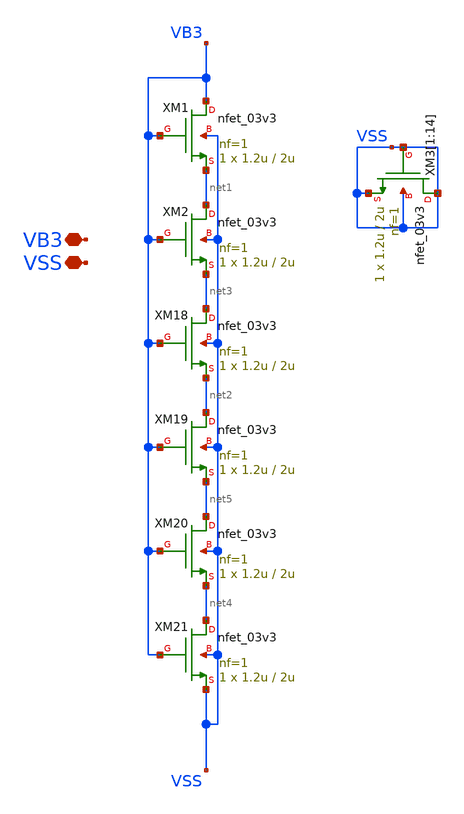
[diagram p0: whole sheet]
** sch_path: TIA_Filter/Folded/FC_bias_vb3.sch
**.subckt FC_bias_vb3 VSS VB3
*.iopin VSS
*.iopin VB3
XM1 VB3 VB3 net1 VSS nfet_03v3 L=2u W=1.2u nf=1 ad='int((nf+1)/2) * W/nf * 0.18u' as='int((nf+2)/2) * W/nf * 0.18u'
+ pd='2*int((nf+1)/2) * (W/nf + 0.18u)' ps='2*int((nf+2)/2) * (W/nf + 0.18u)' nrd='0.18u / W' nrs='0.18u / W'
+ sa=0 sb=0 sd=0 m=1
XM2 net1 VB3 net3 VSS nfet_03v3 L=2u W=1.2u nf=1 ad='int((nf+1)/2) * W/nf * 0.18u' as='int((nf+2)/2) * W/nf * 0.18u'
+ pd='2*int((nf+1)/2) * (W/nf + 0.18u)' ps='2*int((nf+2)/2) * (W/nf + 0.18u)' nrd='0.18u / W' nrs='0.18u / W'
+ sa=0 sb=0 sd=0 m=1
XM18 net3 VB3 net2 VSS nfet_03v3 L=2u W=1.2u nf=1 ad='int((nf+1)/2) * W/nf * 0.18u' as='int((nf+2)/2) * W/nf * 0.18u'
+ pd='2*int((nf+1)/2) * (W/nf + 0.18u)' ps='2*int((nf+2)/2) * (W/nf + 0.18u)' nrd='0.18u / W' nrs='0.18u / W'
+ sa=0 sb=0 sd=0 m=1
XM19 net2 VB3 net5 VSS nfet_03v3 L=2u W=1.2u nf=1 ad='int((nf+1)/2) * W/nf * 0.18u' as='int((nf+2)/2) * W/nf * 0.18u'
+ pd='2*int((nf+1)/2) * (W/nf + 0.18u)' ps='2*int((nf+2)/2) * (W/nf + 0.18u)' nrd='0.18u / W' nrs='0.18u / W'
+ sa=0 sb=0 sd=0 m=1
XM20 net5 VB3 net4 VSS nfet_03v3 L=2u W=1.2u nf=1 ad='int((nf+1)/2) * W/nf * 0.18u' as='int((nf+2)/2) * W/nf * 0.18u'
+ pd='2*int((nf+1)/2) * (W/nf + 0.18u)' ps='2*int((nf+2)/2) * (W/nf + 0.18u)' nrd='0.18u / W' nrs='0.18u / W'
+ sa=0 sb=0 sd=0 m=1
XM21 net4 VB3 VSS VSS nfet_03v3 L=2u W=1.2u nf=1 ad='int((nf+1)/2) * W/nf * 0.18u' as='int((nf+2)/2) * W/nf * 0.18u'
+ pd='2*int((nf+1)/2) * (W/nf + 0.18u)' ps='2*int((nf+2)/2) * (W/nf + 0.18u)' nrd='0.18u / W' nrs='0.18u / W'
+ sa=0 sb=0 sd=0 m=1
XM3[1] VSS VSS VSS VSS nfet_03v3 L=2u W=1.2u nf=1 ad='int((nf+1)/2) * W/nf * 0.18u' as='int((nf+2)/2) * W/nf * 0.18u'
+ pd='2*int((nf+1)/2) * (W/nf + 0.18u)' ps='2*int((nf+2)/2) * (W/nf + 0.18u)' nrd='0.18u / W' nrs='0.18u / W'
+ sa=0 sb=0 sd=0 m=1
XM3[2] VSS VSS VSS VSS nfet_03v3 L=2u W=1.2u nf=1 ad='int((nf+1)/2) * W/nf * 0.18u' as='int((nf+2)/2) * W/nf * 0.18u'
+ pd='2*int((nf+1)/2) * (W/nf + 0.18u)' ps='2*int((nf+2)/2) * (W/nf + 0.18u)' nrd='0.18u / W' nrs='0.18u / W'
+ sa=0 sb=0 sd=0 m=1
XM3[3] VSS VSS VSS VSS nfet_03v3 L=2u W=1.2u nf=1 ad='int((nf+1)/2) * W/nf * 0.18u' as='int((nf+2)/2) * W/nf * 0.18u'
+ pd='2*int((nf+1)/2) * (W/nf + 0.18u)' ps='2*int((nf+2)/2) * (W/nf + 0.18u)' nrd='0.18u / W' nrs='0.18u / W'
+ sa=0 sb=0 sd=0 m=1
XM3[4] VSS VSS VSS VSS nfet_03v3 L=2u W=1.2u nf=1 ad='int((nf+1)/2) * W/nf * 0.18u' as='int((nf+2)/2) * W/nf * 0.18u'
+ pd='2*int((nf+1)/2) * (W/nf + 0.18u)' ps='2*int((nf+2)/2) * (W/nf + 0.18u)' nrd='0.18u / W' nrs='0.18u / W'
+ sa=0 sb=0 sd=0 m=1
XM3[5] VSS VSS VSS VSS nfet_03v3 L=2u W=1.2u nf=1 ad='int((nf+1)/2) * W/nf * 0.18u' as='int((nf+2)/2) * W/nf * 0.18u'
+ pd='2*int((nf+1)/2) * (W/nf + 0.18u)' ps='2*int((nf+2)/2) * (W/nf + 0.18u)' nrd='0.18u / W' nrs='0.18u / W'
+ sa=0 sb=0 sd=0 m=1
XM3[6] VSS VSS VSS VSS nfet_03v3 L=2u W=1.2u nf=1 ad='int((nf+1)/2) * W/nf * 0.18u' as='int((nf+2)/2) * W/nf * 0.18u'
+ pd='2*int((nf+1)/2) * (W/nf + 0.18u)' ps='2*int((nf+2)/2) * (W/nf + 0.18u)' nrd='0.18u / W' nrs='0.18u / W'
+ sa=0 sb=0 sd=0 m=1
XM3[7] VSS VSS VSS VSS nfet_03v3 L=2u W=1.2u nf=1 ad='int((nf+1)/2) * W/nf * 0.18u' as='int((nf+2)/2) * W/nf * 0.18u'
+ pd='2*int((nf+1)/2) * (W/nf + 0.18u)' ps='2*int((nf+2)/2) * (W/nf + 0.18u)' nrd='0.18u / W' nrs='0.18u / W'
+ sa=0 sb=0 sd=0 m=1
XM3[8] VSS VSS VSS VSS nfet_03v3 L=2u W=1.2u nf=1 ad='int((nf+1)/2) * W/nf * 0.18u' as='int((nf+2)/2) * W/nf * 0.18u'
+ pd='2*int((nf+1)/2) * (W/nf + 0.18u)' ps='2*int((nf+2)/2) * (W/nf + 0.18u)' nrd='0.18u / W' nrs='0.18u / W'
+ sa=0 sb=0 sd=0 m=1
XM3[9] VSS VSS VSS VSS nfet_03v3 L=2u W=1.2u nf=1 ad='int((nf+1)/2) * W/nf * 0.18u' as='int((nf+2)/2) * W/nf * 0.18u'
+ pd='2*int((nf+1)/2) * (W/nf + 0.18u)' ps='2*int((nf+2)/2) * (W/nf + 0.18u)' nrd='0.18u / W' nrs='0.18u / W'
+ sa=0 sb=0 sd=0 m=1
XM3[10] VSS VSS VSS VSS nfet_03v3 L=2u W=1.2u nf=1 ad='int((nf+1)/2) * W/nf * 0.18u' as='int((nf+2)/2) * W/nf * 0.18u'
+ pd='2*int((nf+1)/2) * (W/nf + 0.18u)' ps='2*int((nf+2)/2) * (W/nf + 0.18u)' nrd='0.18u / W' nrs='0.18u / W'
+ sa=0 sb=0 sd=0 m=1
XM3[11] VSS VSS VSS VSS nfet_03v3 L=2u W=1.2u nf=1 ad='int((nf+1)/2) * W/nf * 0.18u' as='int((nf+2)/2) * W/nf * 0.18u'
+ pd='2*int((nf+1)/2) * (W/nf + 0.18u)' ps='2*int((nf+2)/2) * (W/nf + 0.18u)' nrd='0.18u / W' nrs='0.18u / W'
+ sa=0 sb=0 sd=0 m=1
XM3[12] VSS VSS VSS VSS nfet_03v3 L=2u W=1.2u nf=1 ad='int((nf+1)/2) * W/nf * 0.18u' as='int((nf+2)/2) * W/nf * 0.18u'
+ pd='2*int((nf+1)/2) * (W/nf + 0.18u)' ps='2*int((nf+2)/2) * (W/nf + 0.18u)' nrd='0.18u / W' nrs='0.18u / W'
+ sa=0 sb=0 sd=0 m=1
XM3[13] VSS VSS VSS VSS nfet_03v3 L=2u W=1.2u nf=1 ad='int((nf+1)/2) * W/nf * 0.18u' as='int((nf+2)/2) * W/nf * 0.18u'
+ pd='2*int((nf+1)/2) * (W/nf + 0.18u)' ps='2*int((nf+2)/2) * (W/nf + 0.18u)' nrd='0.18u / W' nrs='0.18u / W'
+ sa=0 sb=0 sd=0 m=1
XM3[14] VSS VSS VSS VSS nfet_03v3 L=2u W=1.2u nf=1 ad='int((nf+1)/2) * W/nf * 0.18u' as='int((nf+2)/2) * W/nf * 0.18u'
+ pd='2*int((nf+1)/2) * (W/nf + 0.18u)' ps='2*int((nf+2)/2) * (W/nf + 0.18u)' nrd='0.18u / W' nrs='0.18u / W'
+ sa=0 sb=0 sd=0 m=1
**.ends
.end
